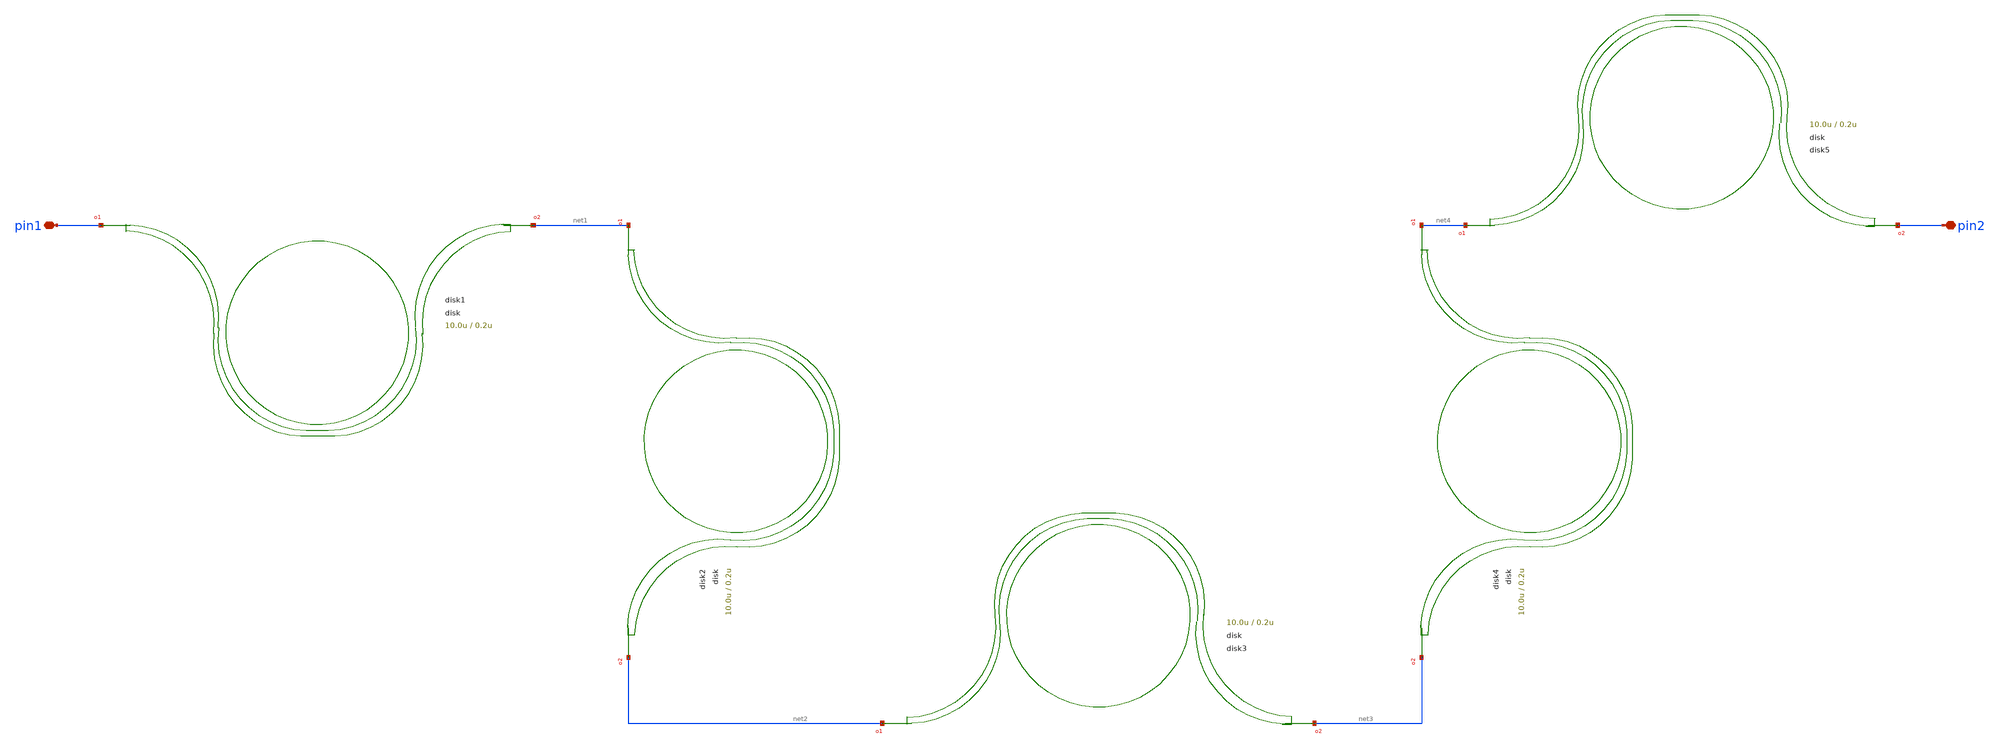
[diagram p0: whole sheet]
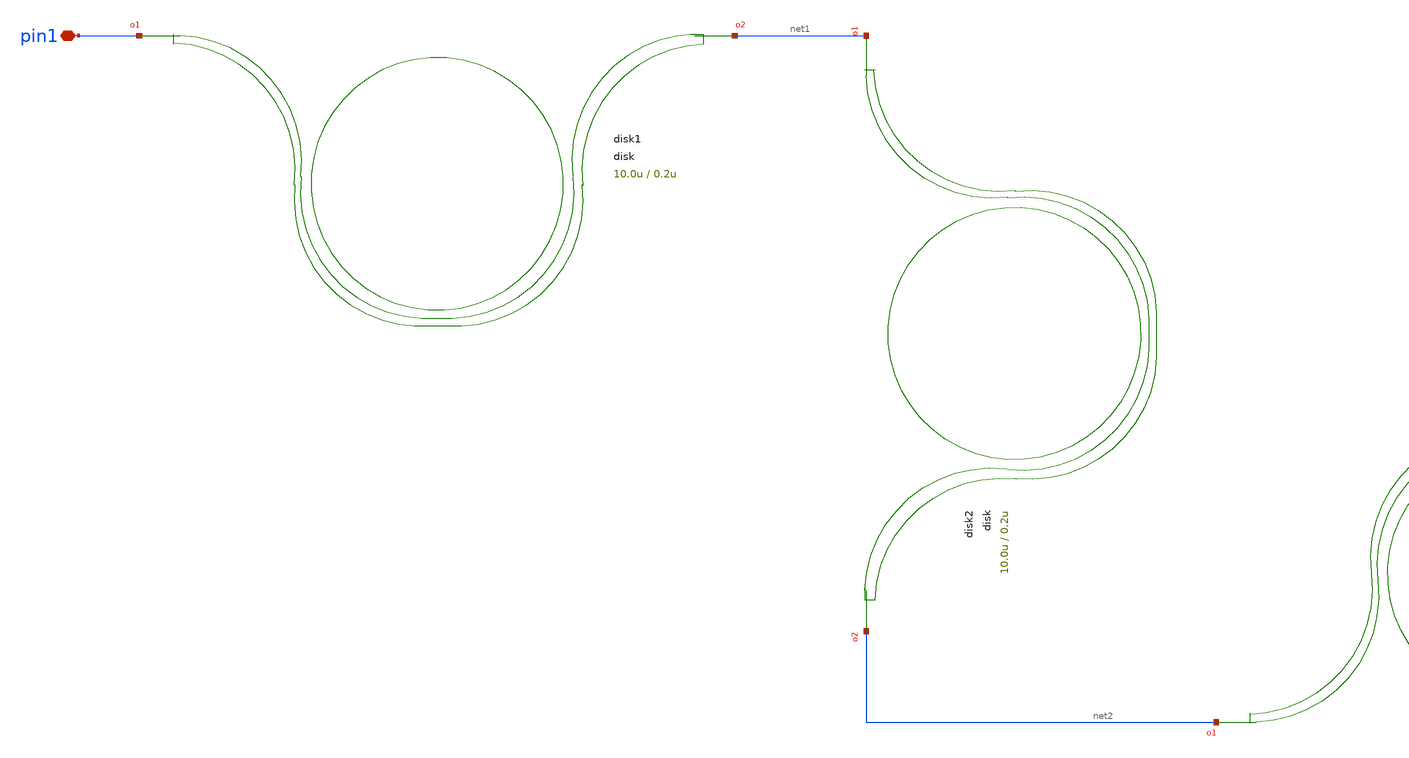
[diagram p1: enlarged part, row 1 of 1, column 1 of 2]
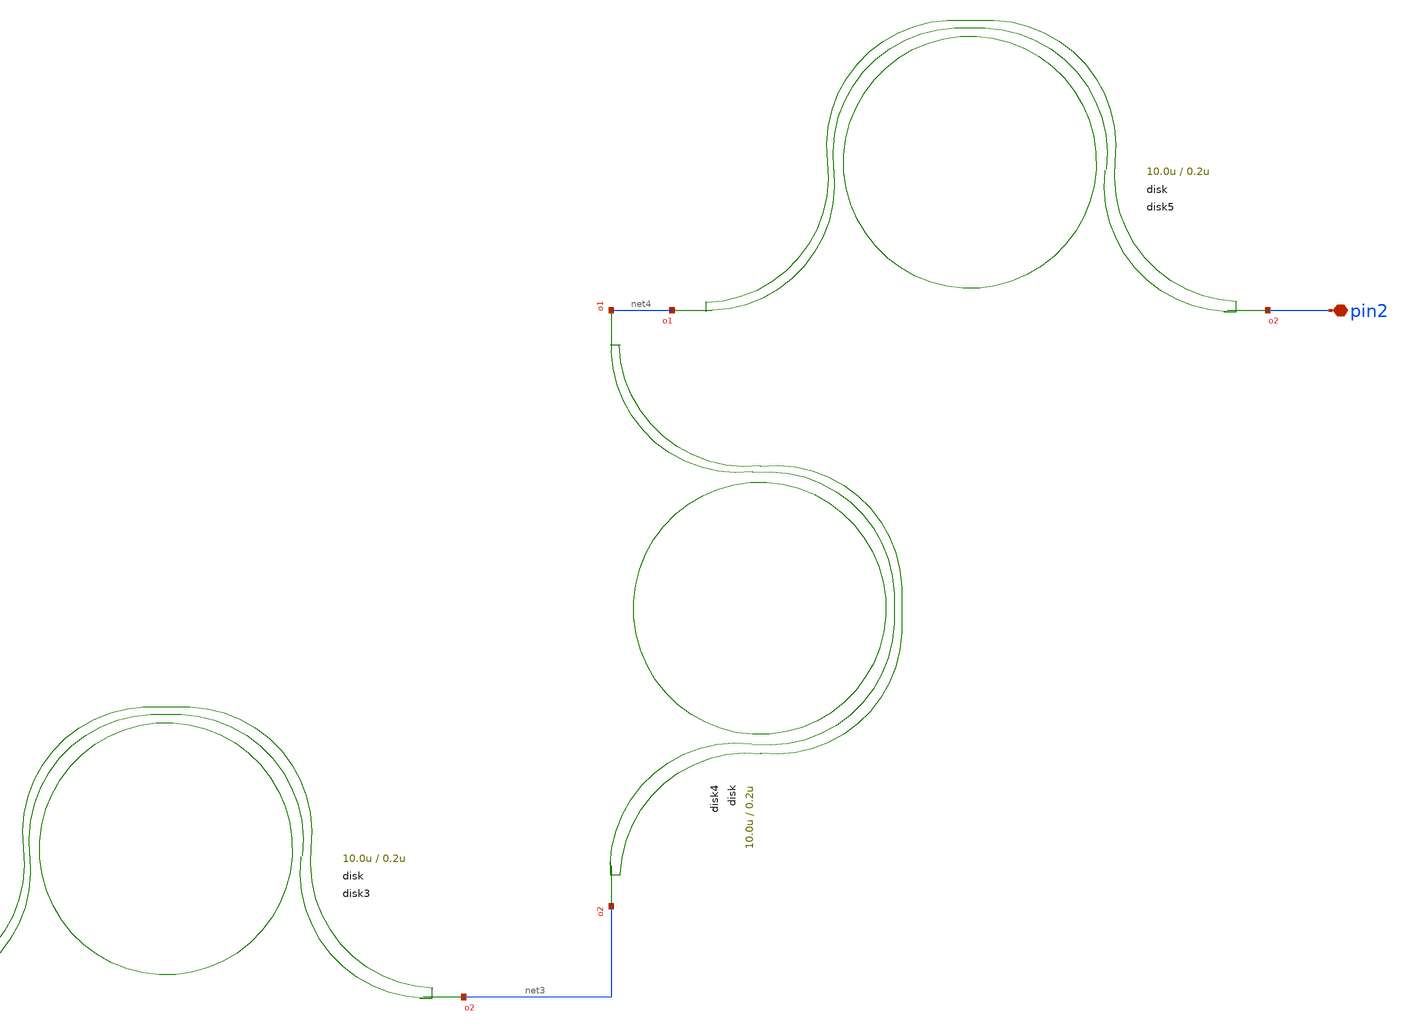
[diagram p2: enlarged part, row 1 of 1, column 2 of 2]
** sch_path: xschem/tests/test_sch/test_disk.sch
* Copyright (c) 2024, Mabrains LLC
* Licensed under the GNU Lesser General Public License, Version 3.0 (the "License");
* you may not use this file except in compliance with the License.
* GNU Lesser General Public License
* Version 3, 29 June 2007
* This program is free software: you can redistribute it and/or modify
* it under the terms of the GNU Lesser General Public License as published
* by the Free Software Foundation, either version 3 of the License, or
* (at your option) any later version.
* This program is distributed in the hope that it will be useful,
* but WITHOUT ANY WARRANTY; without even the implied warranty of
* MERCHANTABILITY or FITNESS FOR A PARTICULAR PURPOSE.  See the
* GNU Lesser General Public License for more details.
* You should have received a copy of the GNU Lesser General Public License
* along with this program.  If not, see <https://www.gnu.org/licenses/>.
* SPDX-License-Identifier: LGPL-3.0
**.subckt test_disk pin1 pin2
*.iopin pin1
*.iopin pin2
Pdisk1 pin1 net1 disk radius=10.0u gap=0.2u wrap_angle_deg=180.0 parity=1
Pdisk2 net1 net2 disk radius=10.0u gap=0.2u wrap_angle_deg=180.0 parity=1
Pdisk3 net2 net3 disk radius=10.0u gap=0.2u wrap_angle_deg=180.0 parity=1
Pdisk4 net4 net3 disk radius=10.0u gap=0.2u wrap_angle_deg=180.0 parity=1
Pdisk5 net4 pin2 disk radius=10.0u gap=0.2u wrap_angle_deg=180.0 parity=1
**.ends
.end
